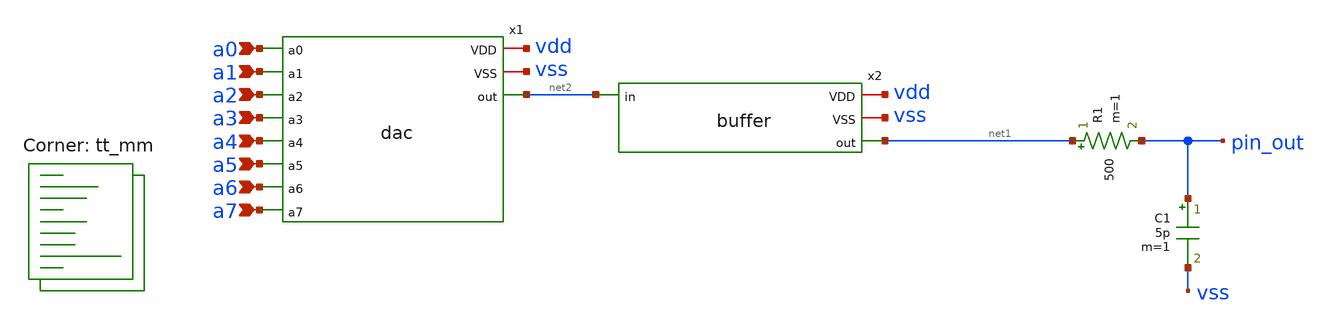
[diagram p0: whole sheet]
** sch_path: xschem/testbench_dac_extremes.sch
**.subckt testbench_dac_extremes a0 a1 a2 a3 a4 a5 a6 a7
*.ipin a0
*.ipin a1
*.ipin a2
*.ipin a3
*.ipin a4
*.ipin a5
*.ipin a6
*.ipin a7
R1 net1 pin_out 500 m=1
C1 pin_out vss 5p m=1
x1 vdd vss a1 a3 a4 a5 a6 a2 a7 a0 net2 dac
x2 vdd vss net1 net2 buffer
**** begin user architecture code



.param VCC=1.8
.param HIGH={VCC}
.param LOW=0

Vvdd vdd 0 {VCC}
Vvss vss 0 0

Va0 a0 0 pwl 0 {LOW} 40n {LOW} 41n {HIGH} 80n {HIGH} 81n {LOW} 120n {LOW}
Va1 a1 0 pwl 0 {LOW} 40n {LOW} 41n {HIGH} 80n {HIGH} 81n {LOW} 120n {LOW}
Va2 a2 0 pwl 0 {LOW} 40n {LOW} 41n {HIGH} 80n {HIGH} 81n {LOW} 120n {LOW}
Va3 a3 0 pwl 0 {LOW} 40n {LOW} 41n {HIGH} 80n {HIGH} 81n {LOW} 120n {LOW}
Va4 a4 0 pwl 0 {LOW} 40n {LOW} 41n {HIGH} 80n {HIGH} 81n {LOW} 120n {LOW}
Va5 a5 0 pwl 0 {LOW} 40n {LOW} 41n {HIGH} 80n {HIGH} 81n {LOW} 120n {LOW}
Va6 a6 0 pwl 0 {LOW} 40n {LOW} 41n {HIGH} 80n {HIGH} 81n {LOW} 120n {LOW}
Va7 a7 0 pwl 0 {LOW} 40n {LOW} 41n {HIGH} 80n {HIGH} 81n {LOW} 120n {LOW}

.control
  repeat 100
    tran 100p 160n
    write testbench_dac_extremes.raw
    set appendwrite
    reset
  end
  quit 0
.endc



.lib $::SKYWATER_MODELS/sky130.lib.spice tt_mm
**** end user architecture code
**.ends

* expanding   symbol:  dac.sym # of pins=11
** sym_path: xschem/dac.sym
** sch_path: xschem/dac.sch
.subckt dac VDD VSS a1 a3 a4 a5 a6 a2 a7 a0 out
*.iopin VSS
*.ipin a0
*.ipin a1
*.ipin a2
*.ipin a3
*.ipin a4
*.ipin a5
*.opin out
*.ipin a6
*.ipin a7
*.iopin VDD
XR1 net1 a0 VSS sky130_fd_pr__res_high_po_0p35 L=40 mult=1 m=1
XR3 VSS net1 VSS sky130_fd_pr__res_high_po_0p35 L=40 mult=1 m=1
XR2 net2 a1 VSS sky130_fd_pr__res_high_po_0p35 L=40 mult=1 m=1
XR4 net1 net2 VSS sky130_fd_pr__res_high_po_0p35 L=20 mult=1 m=1
XR5 net3 a2 VSS sky130_fd_pr__res_high_po_0p35 L=40 mult=1 m=1
XR6 net2 net3 VSS sky130_fd_pr__res_high_po_0p35 L=20 mult=1 m=1
XR7 net4 a3 VSS sky130_fd_pr__res_high_po_0p35 L=40 mult=1 m=1
XR8 net3 net4 VSS sky130_fd_pr__res_high_po_0p35 L=20 mult=1 m=1
XR9 net5 a4 VSS sky130_fd_pr__res_high_po_0p35 L=40 mult=1 m=1
XR10 net4 net5 VSS sky130_fd_pr__res_high_po_0p35 L=20 mult=1 m=1
XR11 net6 a5 VSS sky130_fd_pr__res_high_po_0p35 L=40 mult=1 m=1
XR12 net5 net6 VSS sky130_fd_pr__res_high_po_0p35 L=20 mult=1 m=1
XR13 net7 a6 VSS sky130_fd_pr__res_high_po_0p35 L=40 mult=1 m=1
XR14 net6 net7 VSS sky130_fd_pr__res_high_po_0p35 L=20 mult=1 m=1
XR15 net8 a7 VSS sky130_fd_pr__res_high_po_0p35 L=40 mult=1 m=1
XR16 net7 net8 VSS sky130_fd_pr__res_high_po_0p35 L=20 mult=1 m=1
XR17 out VDD VSS sky130_fd_pr__res_high_po_0p35 L=40 mult=1 m=1
XR18 net8 out VSS sky130_fd_pr__res_high_po_0p35 L=20 mult=1 m=1
.ends


* expanding   symbol:  buffer.sym # of pins=4
** sym_path: xschem/buffer.sym
** sch_path: xschem/buffer.sch
.subckt buffer VDD VSS out in
*.iopin VSS
*.iopin VDD
*.ipin in
*.opin out
XM3 VDD in out VSS sky130_fd_pr__nfet_01v8_lvt L=0.15 W=7 nf=1 ad='int((nf+1)/2) * W/nf * 0.29' as='int((nf+2)/2) * W/nf * 0.29'
+ pd='2*int((nf+1)/2) * (W/nf + 0.29)' ps='2*int((nf+2)/2) * (W/nf + 0.29)' nrd='0.29 / W' nrs='0.29 / W'
+ sa=0 sb=0 sd=0 mult=1 m=1
XM1 out net1 VSS VSS sky130_fd_pr__nfet_01v8_lvt L=0.15 W=7 nf=1 ad='int((nf+1)/2) * W/nf * 0.29' as='int((nf+2)/2) * W/nf * 0.29'
+ pd='2*int((nf+1)/2) * (W/nf + 0.29)' ps='2*int((nf+2)/2) * (W/nf + 0.29)' nrd='0.29 / W' nrs='0.29 / W'
+ sa=0 sb=0 sd=0 mult=1 m=1
XR5 VSS net1 VSS sky130_fd_pr__res_high_po_0p35 L=40 mult=1 m=1
XR6 net1 VDD VSS sky130_fd_pr__res_high_po_0p35 L=20 mult=1 m=1
.ends

.end
